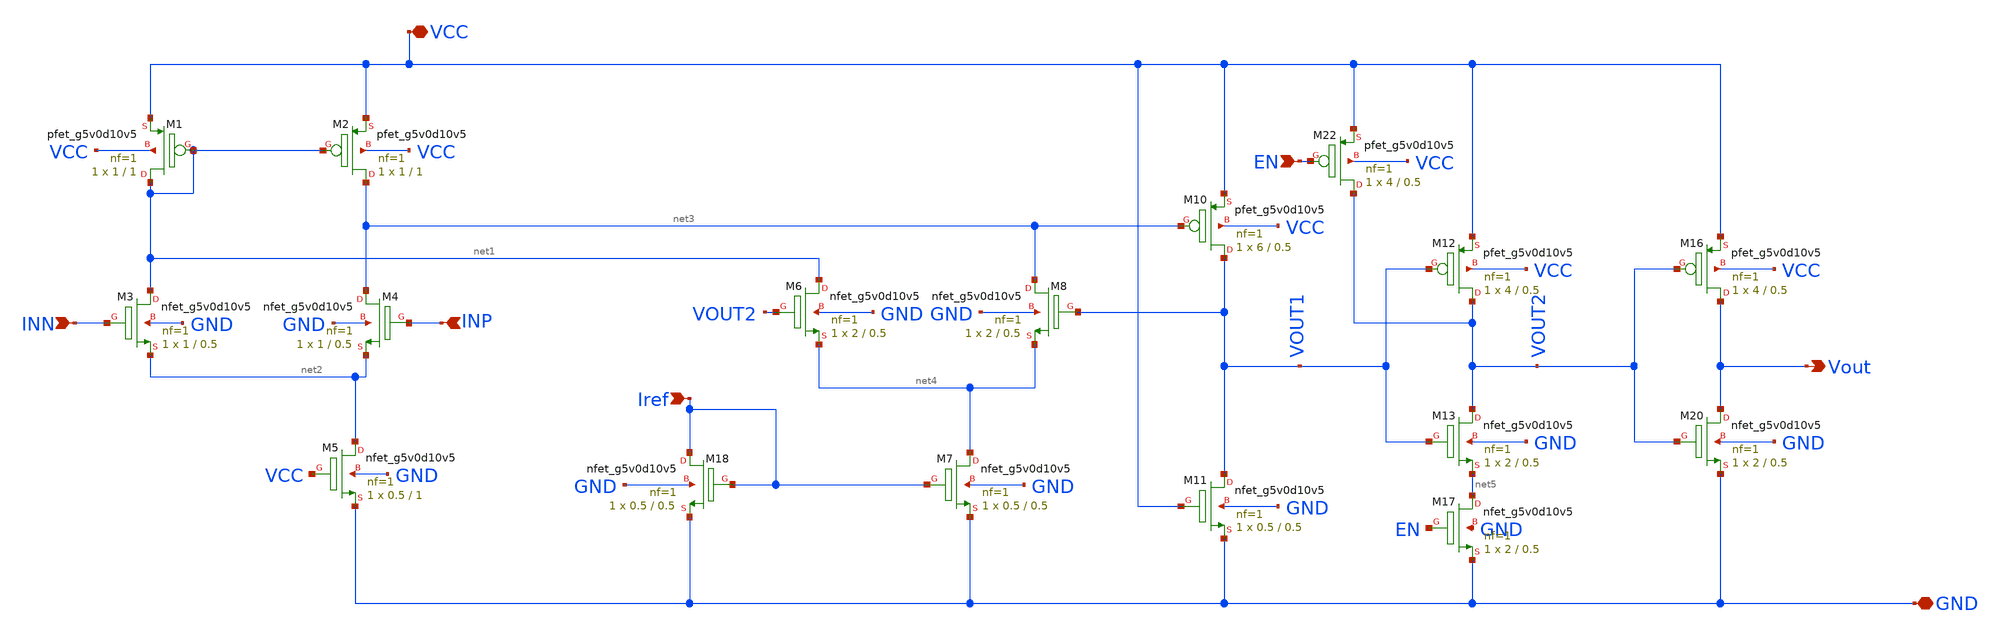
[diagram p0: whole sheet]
** sch_path: week8/Prelayout/compen.sch
**.subckt compen INN INP EN VCC GND Vout Iref
*.ipin INN
*.ipin INP
*.ipin EN
*.iopin VCC
*.iopin GND
*.opin Vout
*.ipin Iref
XM2 net3 net1 VCC VCC sky130_fd_pr__pfet_g5v0d10v5 L=1 W=1 nf=1 ad='int((nf+1)/2) * W/nf * 0.29' as='int((nf+2)/2) * W/nf * 0.29'
+ pd='2*int((nf+1)/2) * (W/nf + 0.29)' ps='2*int((nf+2)/2) * (W/nf + 0.29)' nrd='0.29 / W' nrs='0.29 / W'
+ sa=0 sb=0 sd=0 mult=1 m=1
XM1 net1 net1 VCC VCC sky130_fd_pr__pfet_g5v0d10v5 L=1 W=1 nf=1 ad='int((nf+1)/2) * W/nf * 0.29' as='int((nf+2)/2) * W/nf * 0.29'
+ pd='2*int((nf+1)/2) * (W/nf + 0.29)' ps='2*int((nf+2)/2) * (W/nf + 0.29)' nrd='0.29 / W' nrs='0.29 / W'
+ sa=0 sb=0 sd=0 mult=1 m=1
XM12 VOUT2 VOUT1 VCC VCC sky130_fd_pr__pfet_g5v0d10v5 L=0.5 W=4 nf=1 ad='int((nf+1)/2) * W/nf * 0.29'
+ as='int((nf+2)/2) * W/nf * 0.29' pd='2*int((nf+1)/2) * (W/nf + 0.29)' ps='2*int((nf+2)/2) * (W/nf + 0.29)'
+ nrd='0.29 / W' nrs='0.29 / W' sa=0 sb=0 sd=0 mult=1 m=1
XM10 VOUT1 net3 VCC VCC sky130_fd_pr__pfet_g5v0d10v5 L=0.5 W=6 nf=1 ad='int((nf+1)/2) * W/nf * 0.29'
+ as='int((nf+2)/2) * W/nf * 0.29' pd='2*int((nf+1)/2) * (W/nf + 0.29)' ps='2*int((nf+2)/2) * (W/nf + 0.29)'
+ nrd='0.29 / W' nrs='0.29 / W' sa=0 sb=0 sd=0 mult=1 m=1
XM16 Vout VOUT2 VCC VCC sky130_fd_pr__pfet_g5v0d10v5 L=0.5 W=4 nf=1 ad='int((nf+1)/2) * W/nf * 0.29'
+ as='int((nf+2)/2) * W/nf * 0.29' pd='2*int((nf+1)/2) * (W/nf + 0.29)' ps='2*int((nf+2)/2) * (W/nf + 0.29)'
+ nrd='0.29 / W' nrs='0.29 / W' sa=0 sb=0 sd=0 mult=1 m=1
XM22 VOUT2 EN VCC VCC sky130_fd_pr__pfet_g5v0d10v5 L=0.5 W=4 nf=1 ad='int((nf+1)/2) * W/nf * 0.29' as='int((nf+2)/2) * W/nf * 0.29'
+ pd='2*int((nf+1)/2) * (W/nf + 0.29)' ps='2*int((nf+2)/2) * (W/nf + 0.29)' nrd='0.29 / W' nrs='0.29 / W'
+ sa=0 sb=0 sd=0 mult=1 m=1
XM20 Vout VOUT2 GND GND sky130_fd_pr__nfet_g5v0d10v5 L=0.5 W=2 nf=1 ad='int((nf+1)/2) * W/nf * 0.29'
+ as='int((nf+2)/2) * W/nf * 0.29' pd='2*int((nf+1)/2) * (W/nf + 0.29)' ps='2*int((nf+2)/2) * (W/nf + 0.29)'
+ nrd='0.29 / W' nrs='0.29 / W' sa=0 sb=0 sd=0 mult=1 m=1
XM17 net5 EN GND GND sky130_fd_pr__nfet_g5v0d10v5 L=0.5 W=2 nf=1 ad='int((nf+1)/2) * W/nf * 0.29' as='int((nf+2)/2) * W/nf * 0.29'
+ pd='2*int((nf+1)/2) * (W/nf + 0.29)' ps='2*int((nf+2)/2) * (W/nf + 0.29)' nrd='0.29 / W' nrs='0.29 / W'
+ sa=0 sb=0 sd=0 mult=1 m=1
XM13 VOUT2 VOUT1 net5 GND sky130_fd_pr__nfet_g5v0d10v5 L=0.5 W=2 nf=1 ad='int((nf+1)/2) * W/nf * 0.29'
+ as='int((nf+2)/2) * W/nf * 0.29' pd='2*int((nf+1)/2) * (W/nf + 0.29)' ps='2*int((nf+2)/2) * (W/nf + 0.29)'
+ nrd='0.29 / W' nrs='0.29 / W' sa=0 sb=0 sd=0 mult=1 m=1
XM11 VOUT1 VCC GND GND sky130_fd_pr__nfet_g5v0d10v5 L=0.5 W=0.5 nf=1 ad='int((nf+1)/2) * W/nf * 0.29'
+ as='int((nf+2)/2) * W/nf * 0.29' pd='2*int((nf+1)/2) * (W/nf + 0.29)' ps='2*int((nf+2)/2) * (W/nf + 0.29)'
+ nrd='0.29 / W' nrs='0.29 / W' sa=0 sb=0 sd=0 mult=1 m=1
XM7 net4 Iref GND GND sky130_fd_pr__nfet_g5v0d10v5 L=0.5 W=0.5 nf=1 ad='int((nf+1)/2) * W/nf * 0.29'
+ as='int((nf+2)/2) * W/nf * 0.29' pd='2*int((nf+1)/2) * (W/nf + 0.29)' ps='2*int((nf+2)/2) * (W/nf + 0.29)'
+ nrd='0.29 / W' nrs='0.29 / W' sa=0 sb=0 sd=0 mult=1 m=1
XM18 Iref Iref GND GND sky130_fd_pr__nfet_g5v0d10v5 L=0.5 W=0.5 nf=1 ad='int((nf+1)/2) * W/nf * 0.29'
+ as='int((nf+2)/2) * W/nf * 0.29' pd='2*int((nf+1)/2) * (W/nf + 0.29)' ps='2*int((nf+2)/2) * (W/nf + 0.29)'
+ nrd='0.29 / W' nrs='0.29 / W' sa=0 sb=0 sd=0 mult=1 m=1
XM6 net1 VOUT2 net4 GND sky130_fd_pr__nfet_g5v0d10v5 L=0.5 W=2 nf=1 ad='int((nf+1)/2) * W/nf * 0.29'
+ as='int((nf+2)/2) * W/nf * 0.29' pd='2*int((nf+1)/2) * (W/nf + 0.29)' ps='2*int((nf+2)/2) * (W/nf + 0.29)'
+ nrd='0.29 / W' nrs='0.29 / W' sa=0 sb=0 sd=0 mult=1 m=1
XM8 net3 VOUT1 net4 GND sky130_fd_pr__nfet_g5v0d10v5 L=0.5 W=2 nf=1 ad='int((nf+1)/2) * W/nf * 0.29'
+ as='int((nf+2)/2) * W/nf * 0.29' pd='2*int((nf+1)/2) * (W/nf + 0.29)' ps='2*int((nf+2)/2) * (W/nf + 0.29)'
+ nrd='0.29 / W' nrs='0.29 / W' sa=0 sb=0 sd=0 mult=1 m=1
XM5 net2 VCC GND GND sky130_fd_pr__nfet_g5v0d10v5 L=1 W=0.5 nf=1 ad='int((nf+1)/2) * W/nf * 0.29' as='int((nf+2)/2) * W/nf * 0.29'
+ pd='2*int((nf+1)/2) * (W/nf + 0.29)' ps='2*int((nf+2)/2) * (W/nf + 0.29)' nrd='0.29 / W' nrs='0.29 / W'
+ sa=0 sb=0 sd=0 mult=1 m=1
XM3 net1 INN net2 GND sky130_fd_pr__nfet_g5v0d10v5 L=0.5 W=1 nf=1 ad='int((nf+1)/2) * W/nf * 0.29' as='int((nf+2)/2) * W/nf * 0.29'
+ pd='2*int((nf+1)/2) * (W/nf + 0.29)' ps='2*int((nf+2)/2) * (W/nf + 0.29)' nrd='0.29 / W' nrs='0.29 / W'
+ sa=0 sb=0 sd=0 mult=1 m=1
XM4 net3 INP net2 GND sky130_fd_pr__nfet_g5v0d10v5 L=0.5 W=1 nf=1 ad='int((nf+1)/2) * W/nf * 0.29' as='int((nf+2)/2) * W/nf * 0.29'
+ pd='2*int((nf+1)/2) * (W/nf + 0.29)' ps='2*int((nf+2)/2) * (W/nf + 0.29)' nrd='0.29 / W' nrs='0.29 / W'
+ sa=0 sb=0 sd=0 mult=1 m=1
**.ends
.end
